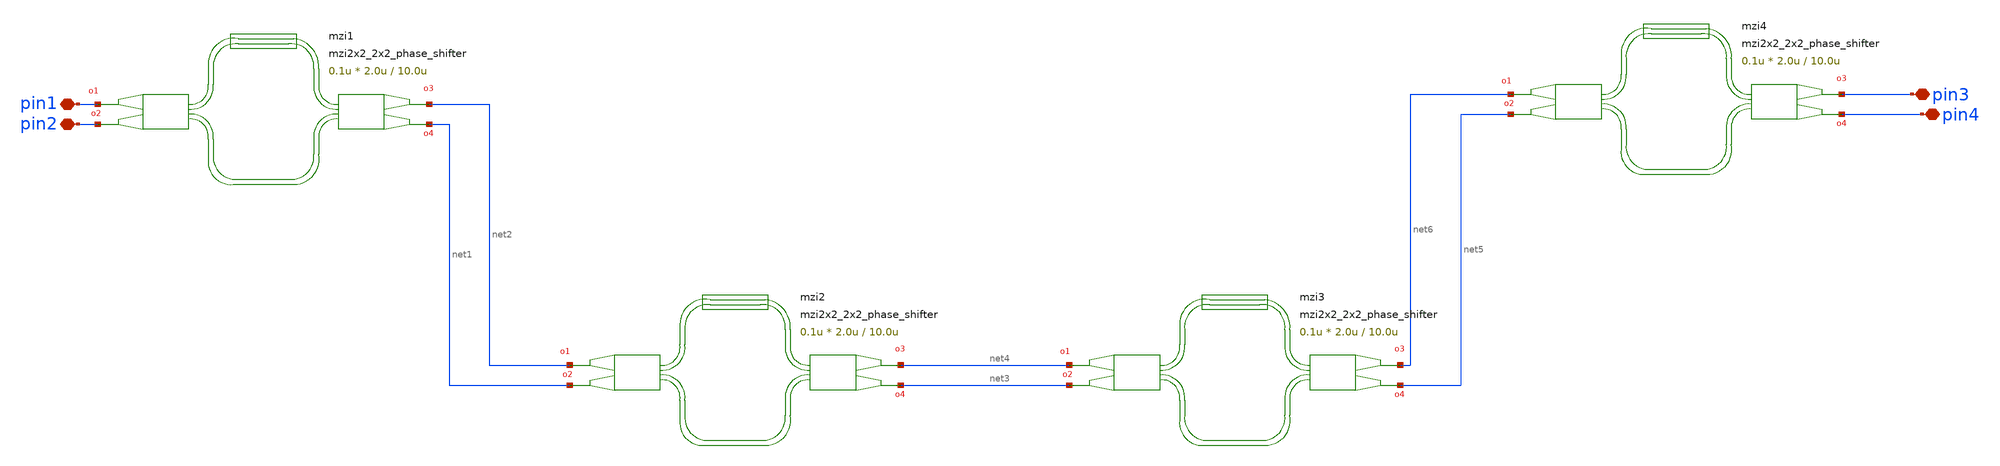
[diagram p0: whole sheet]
** sch_path: xschem/tests/test_sch/test_mzi2x2_2x2_phase_shifter.sch
* Copyright (c) 2024, Mabrains LLC
* Licensed under the GNU Lesser General Public License, Version 3.0 (the "License");
* you may not use this file except in compliance with the License.
* GNU Lesser General Public License
* Version 3, 29 June 2007
* This program is free software: you can redistribute it and/or modify
* it under the terms of the GNU Lesser General Public License as published
* by the Free Software Foundation, either version 3 of the License, or
* (at your option) any later version.
* This program is distributed in the hope that it will be useful,
* but WITHOUT ANY WARRANTY; without even the implied warranty of
* MERCHANTABILITY or FITNESS FOR A PARTICULAR PURPOSE.  See the
* GNU Lesser General Public License for more details.
* You should have received a copy of the GNU Lesser General Public License
* along with this program.  If not, see <https://www.gnu.org/licenses/>.
* SPDX-License-Identifier: LGPL-3.0
**.subckt test_mzi2x2_2x2_phase_shifter pin2 pin1 pin3 pin4
*.iopin pin2
*.iopin pin1
*.iopin pin3
*.iopin pin4
Pmzi1 pin1 pin2 net2 net1 mzi2x2_2x2_phase_shifter delta_length=10.0u length_y=2.0u length_x=0.1u
Pmzi2 net2 net1 net4 net3 mzi2x2_2x2_phase_shifter delta_length=10.0u length_y=2.0u length_x=0.1u
Pmzi3 net4 net3 net6 net5 mzi2x2_2x2_phase_shifter delta_length=10.0u length_y=2.0u length_x=0.1u
Pmzi4 net6 net5 pin3 pin4 mzi2x2_2x2_phase_shifter delta_length=10.0u length_y=2.0u length_x=0.1u
**.ends
.end
